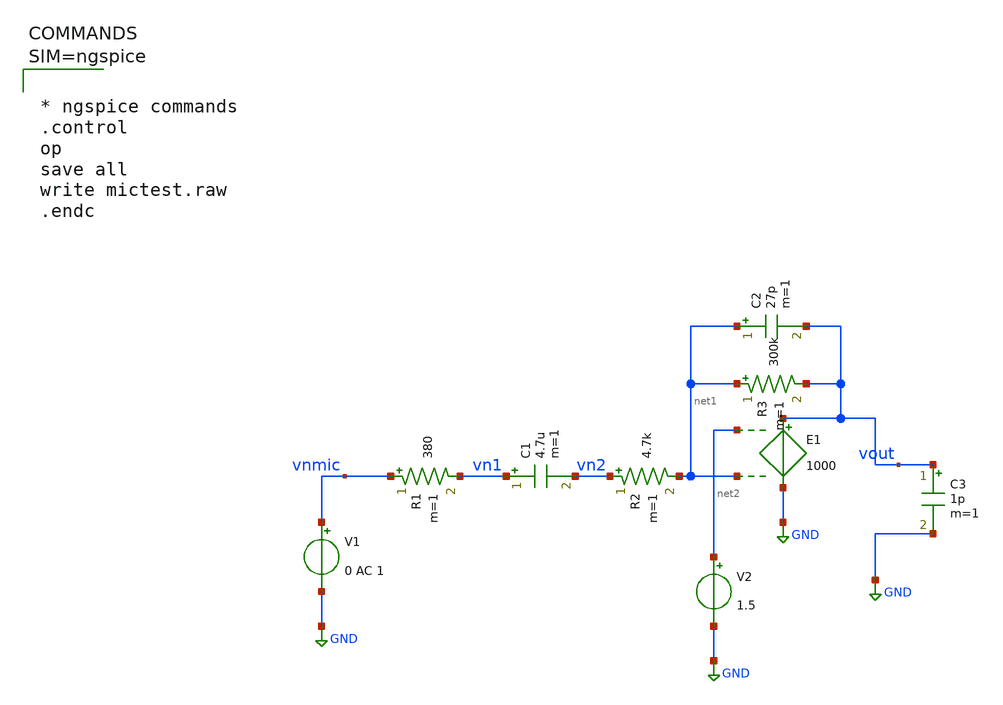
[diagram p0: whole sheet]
** sch_path: xschem/mictest.sch
**.subckt mictest
V1 vnmic GND 0 AC 1
R1 vnmic vn1 380 m=1
C1 vn1 vn2 4.7u m=1
R2 vn2 net1 4.7k m=1
R3 net1 vout 300k m=1
C2 net1 vout 27p m=1
C3 vout GND 1p m=1
E1 vout GND net2 net1 1000
V2 net2 GND 1.5
**** begin user architecture code



* ngspice commands
.control
op
save all
write mictest.raw
.endc



**** end user architecture code
**.ends
.GLOBAL GND
.end
